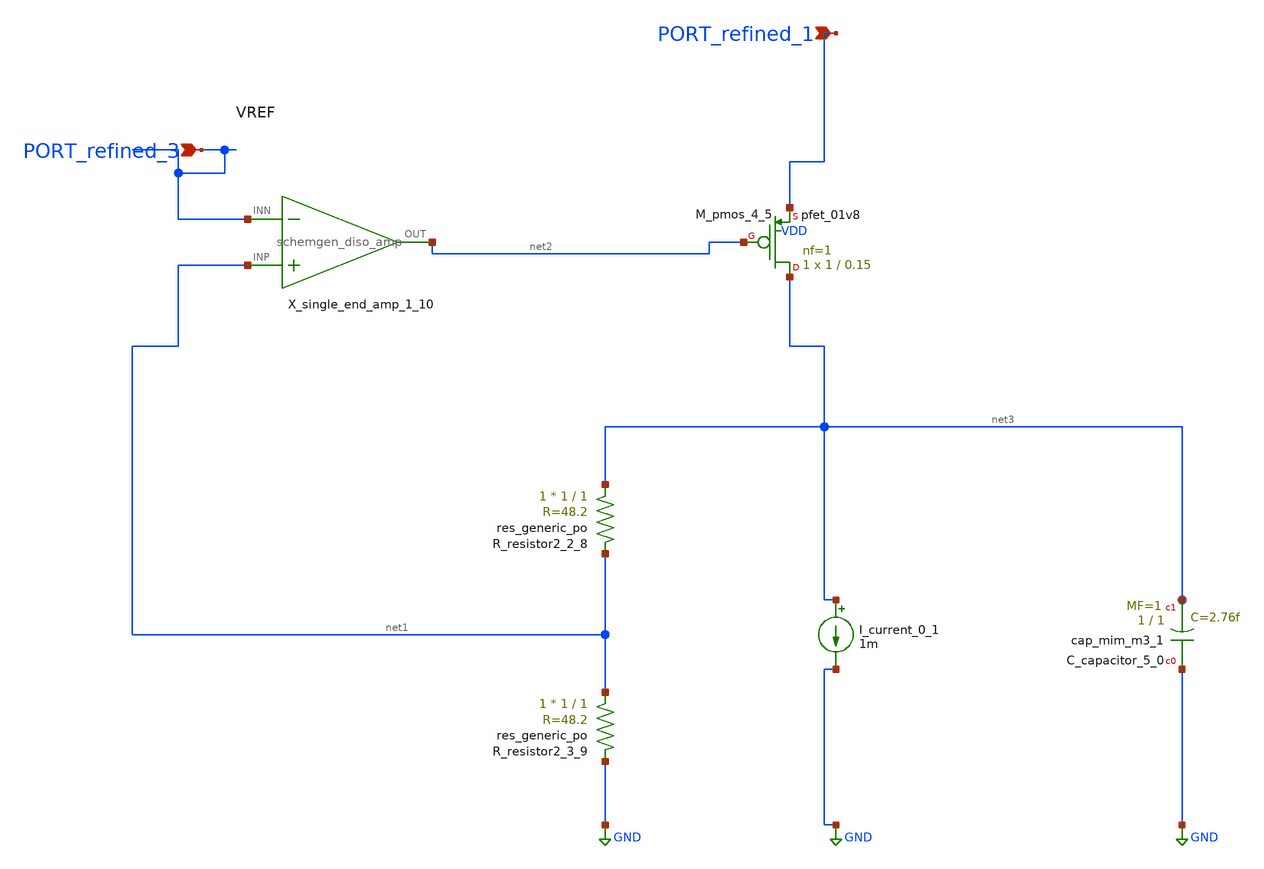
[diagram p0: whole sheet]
** sch_path: schematics/Image2Net/079.sch
**.subckt 079 PORT_refined_3 PORT_refined_1
*.ipin PORT_refined_3
*.ipin PORT_refined_1
XC_capacitor_5_0 GND net3 sky130_fd_pr__cap_mim_m3_1 W=1 L=1 MF=1 m=1
I_current_0_1 net3 GND 1m
XM_pmos_4_5 net3 net2 PORT_refined_1 VDD sky130_fd_pr__pfet_01v8 L=0.15 W=1 nf=1 ad='int((1 + 1)/2) * 1 / 1 * 0.29'
+ as='int((1 + 2)/2) * 1 / 1 * 0.29' pd='2*int((1 + 1)/2) * (1 / 1 + 0.29)' ps='2*int((1 + 2)/2) * (1 / 1 + 0.29)'
+ nrd='0.29 / 1 ' nrs='0.29 / 1 ' sa=0 sb=0 sd=0 mult=1 m=1
XR_resistor2_2_8 net3 net1 sky130_fd_pr__res_generic_po W=1 L=1 m=1
XR_resistor2_3_9 net1 GND sky130_fd_pr__res_generic_po W=1 L=1 m=1
X_single_end_amp_1_10 net1 PORT_refined_3 net2 schemgen_diso_amp
**.ends

* expanding   symbol:  schemgen_diso_amp.sym # of pins=3
** sym_path: symbols/schemgen_diso_amp.sym
.subckt schemgen_diso_amp INP INN OUT
* SchemGen ideal op-amp: Vout = 1e5 * (V(INP) - V(INN))
E1 OUT 0 INP INN 1e5
.ends schemgen_diso_amp
.GLOBAL GND
.end
